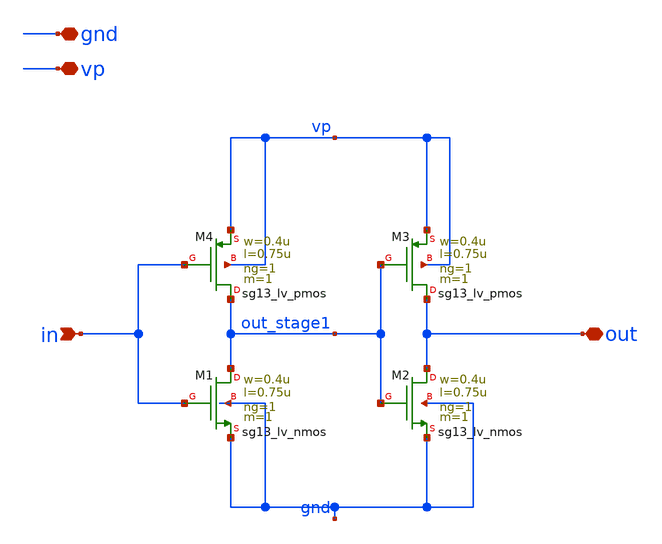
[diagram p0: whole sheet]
** sch_path: PLL0663-main/schematic/xschem/PFD/PFD_buffor.sch
**.subckt PFD_buffor gnd vp in out
*.iopin gnd
*.iopin vp
*.ipin in
*.iopin out
XM1 out_stage1 in gnd gnd sg13_lv_nmos w=0.4u l=0.75u ng=1 m=1 mm_ok=1
XM4 out_stage1 in vp vp sg13_lv_pmos w=0.4u l=0.75u ng=1 m=1 mm_ok=1
XM2 out out_stage1 gnd gnd sg13_lv_nmos w=0.4u l=0.75u ng=1 m=1 mm_ok=1
XM3 out out_stage1 vp vp sg13_lv_pmos w=0.4u l=0.75u ng=1 m=1 mm_ok=1
**.ends
.end
